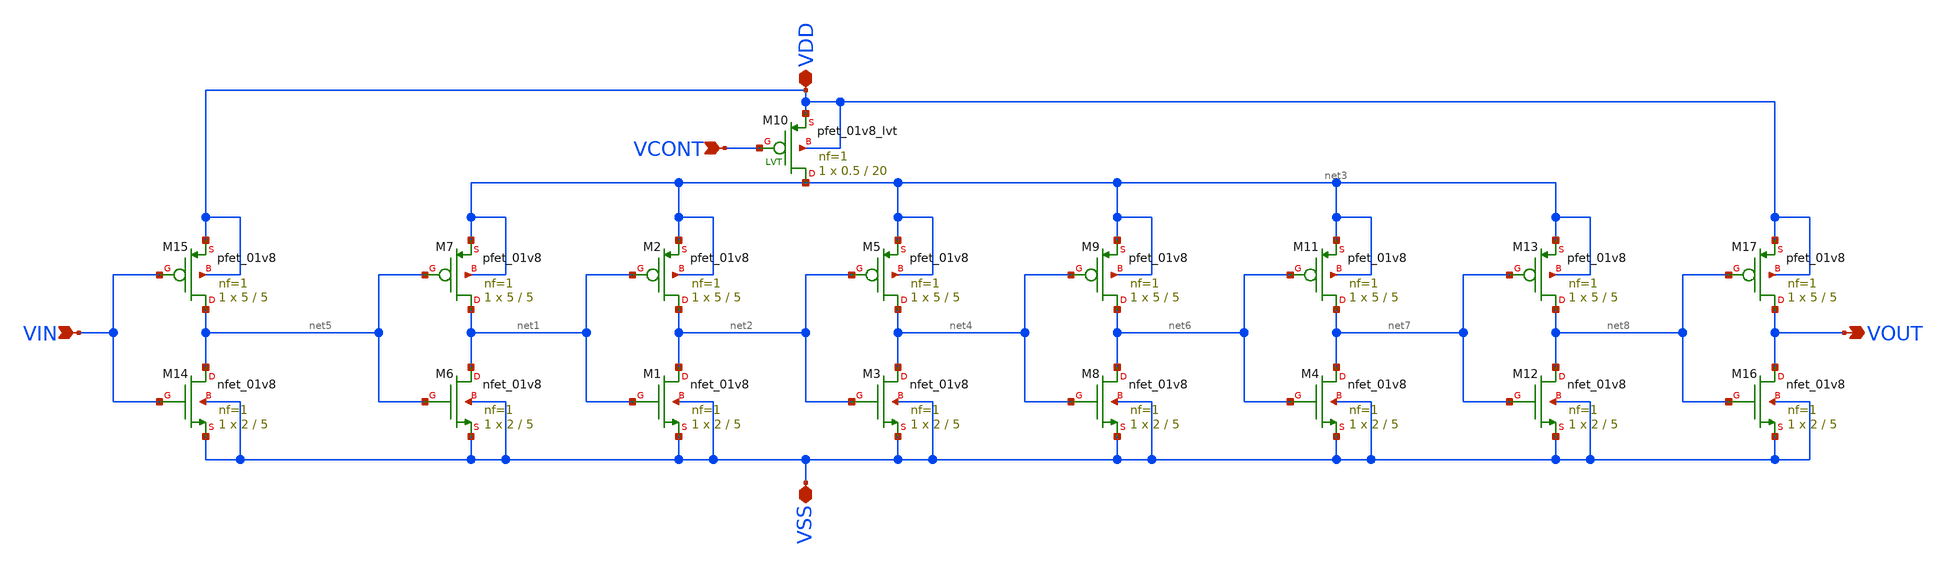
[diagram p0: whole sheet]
** sch_path: xschem/VCDL_HD_v2p1.sch
**.subckt VCDL_HD_v2p1 VIN VOUT VDD VSS VCONT
*.ipin VIN
*.opin VOUT
*.iopin VDD
*.iopin VSS
*.ipin VCONT
XM1 net2 net1 VSS VSS sky130_fd_pr__nfet_01v8 L=5 W=2 nf=1 ad='int((nf+1)/2) * W/nf * 0.29' as='int((nf+2)/2) * W/nf * 0.29'
+ pd='2*int((nf+1)/2) * (W/nf + 0.29)' ps='2*int((nf+2)/2) * (W/nf + 0.29)' nrd='0.29 / W' nrs='0.29 / W'
+ sa=0 sb=0 sd=0 mult=1 m=1
XM2 net2 net1 net3 net3 sky130_fd_pr__pfet_01v8 L=5 W=5 nf=1 ad='int((nf+1)/2) * W/nf * 0.29' as='int((nf+2)/2) * W/nf * 0.29'
+ pd='2*int((nf+1)/2) * (W/nf + 0.29)' ps='2*int((nf+2)/2) * (W/nf + 0.29)' nrd='0.29 / W' nrs='0.29 / W'
+ sa=0 sb=0 sd=0 mult=1 m=1
XM3 net4 net2 VSS VSS sky130_fd_pr__nfet_01v8 L=5 W=2 nf=1 ad='int((nf+1)/2) * W/nf * 0.29' as='int((nf+2)/2) * W/nf * 0.29'
+ pd='2*int((nf+1)/2) * (W/nf + 0.29)' ps='2*int((nf+2)/2) * (W/nf + 0.29)' nrd='0.29 / W' nrs='0.29 / W'
+ sa=0 sb=0 sd=0 mult=1 m=1
XM5 net4 net2 net3 net3 sky130_fd_pr__pfet_01v8 L=5 W=5 nf=1 ad='int((nf+1)/2) * W/nf * 0.29' as='int((nf+2)/2) * W/nf * 0.29'
+ pd='2*int((nf+1)/2) * (W/nf + 0.29)' ps='2*int((nf+2)/2) * (W/nf + 0.29)' nrd='0.29 / W' nrs='0.29 / W'
+ sa=0 sb=0 sd=0 mult=1 m=1
XM6 net1 net5 VSS VSS sky130_fd_pr__nfet_01v8 L=5 W=2 nf=1 ad='int((nf+1)/2) * W/nf * 0.29' as='int((nf+2)/2) * W/nf * 0.29'
+ pd='2*int((nf+1)/2) * (W/nf + 0.29)' ps='2*int((nf+2)/2) * (W/nf + 0.29)' nrd='0.29 / W' nrs='0.29 / W'
+ sa=0 sb=0 sd=0 mult=1 m=1
XM7 net1 net5 net3 net3 sky130_fd_pr__pfet_01v8 L=5 W=5 nf=1 ad='int((nf+1)/2) * W/nf * 0.29' as='int((nf+2)/2) * W/nf * 0.29'
+ pd='2*int((nf+1)/2) * (W/nf + 0.29)' ps='2*int((nf+2)/2) * (W/nf + 0.29)' nrd='0.29 / W' nrs='0.29 / W'
+ sa=0 sb=0 sd=0 mult=1 m=1
XM8 net6 net4 VSS VSS sky130_fd_pr__nfet_01v8 L=5 W=2 nf=1 ad='int((nf+1)/2) * W/nf * 0.29' as='int((nf+2)/2) * W/nf * 0.29'
+ pd='2*int((nf+1)/2) * (W/nf + 0.29)' ps='2*int((nf+2)/2) * (W/nf + 0.29)' nrd='0.29 / W' nrs='0.29 / W'
+ sa=0 sb=0 sd=0 mult=1 m=1
XM9 net6 net4 net3 net3 sky130_fd_pr__pfet_01v8 L=5 W=5 nf=1 ad='int((nf+1)/2) * W/nf * 0.29' as='int((nf+2)/2) * W/nf * 0.29'
+ pd='2*int((nf+1)/2) * (W/nf + 0.29)' ps='2*int((nf+2)/2) * (W/nf + 0.29)' nrd='0.29 / W' nrs='0.29 / W'
+ sa=0 sb=0 sd=0 mult=1 m=1
XM10 net3 VCONT VDD VDD sky130_fd_pr__pfet_01v8_lvt L=20 W=0.5 nf=1 ad='int((nf+1)/2) * W/nf * 0.29'
+ as='int((nf+2)/2) * W/nf * 0.29' pd='2*int((nf+1)/2) * (W/nf + 0.29)' ps='2*int((nf+2)/2) * (W/nf + 0.29)'
+ nrd='0.29 / W' nrs='0.29 / W' sa=0 sb=0 sd=0 mult=1 m=1
XM4 net7 net6 VSS VSS sky130_fd_pr__nfet_01v8 L=5 W=2 nf=1 ad='int((nf+1)/2) * W/nf * 0.29' as='int((nf+2)/2) * W/nf * 0.29'
+ pd='2*int((nf+1)/2) * (W/nf + 0.29)' ps='2*int((nf+2)/2) * (W/nf + 0.29)' nrd='0.29 / W' nrs='0.29 / W'
+ sa=0 sb=0 sd=0 mult=1 m=1
XM11 net7 net6 net3 net3 sky130_fd_pr__pfet_01v8 L=5 W=5 nf=1 ad='int((nf+1)/2) * W/nf * 0.29' as='int((nf+2)/2) * W/nf * 0.29'
+ pd='2*int((nf+1)/2) * (W/nf + 0.29)' ps='2*int((nf+2)/2) * (W/nf + 0.29)' nrd='0.29 / W' nrs='0.29 / W'
+ sa=0 sb=0 sd=0 mult=1 m=1
XM12 net8 net7 VSS VSS sky130_fd_pr__nfet_01v8 L=5 W=2 nf=1 ad='int((nf+1)/2) * W/nf * 0.29' as='int((nf+2)/2) * W/nf * 0.29'
+ pd='2*int((nf+1)/2) * (W/nf + 0.29)' ps='2*int((nf+2)/2) * (W/nf + 0.29)' nrd='0.29 / W' nrs='0.29 / W'
+ sa=0 sb=0 sd=0 mult=1 m=1
XM13 net8 net7 net3 net3 sky130_fd_pr__pfet_01v8 L=5 W=5 nf=1 ad='int((nf+1)/2) * W/nf * 0.29' as='int((nf+2)/2) * W/nf * 0.29'
+ pd='2*int((nf+1)/2) * (W/nf + 0.29)' ps='2*int((nf+2)/2) * (W/nf + 0.29)' nrd='0.29 / W' nrs='0.29 / W'
+ sa=0 sb=0 sd=0 mult=1 m=1
XM14 net5 VIN VSS VSS sky130_fd_pr__nfet_01v8 L=5 W=2 nf=1 ad='int((nf+1)/2) * W/nf * 0.29' as='int((nf+2)/2) * W/nf * 0.29'
+ pd='2*int((nf+1)/2) * (W/nf + 0.29)' ps='2*int((nf+2)/2) * (W/nf + 0.29)' nrd='0.29 / W' nrs='0.29 / W'
+ sa=0 sb=0 sd=0 mult=1 m=1
XM15 net5 VIN VDD VDD sky130_fd_pr__pfet_01v8 L=5 W=5 nf=1 ad='int((nf+1)/2) * W/nf * 0.29' as='int((nf+2)/2) * W/nf * 0.29'
+ pd='2*int((nf+1)/2) * (W/nf + 0.29)' ps='2*int((nf+2)/2) * (W/nf + 0.29)' nrd='0.29 / W' nrs='0.29 / W'
+ sa=0 sb=0 sd=0 mult=1 m=1
XM16 VOUT net8 VSS VSS sky130_fd_pr__nfet_01v8 L=5 W=2 nf=1 ad='int((nf+1)/2) * W/nf * 0.29' as='int((nf+2)/2) * W/nf * 0.29'
+ pd='2*int((nf+1)/2) * (W/nf + 0.29)' ps='2*int((nf+2)/2) * (W/nf + 0.29)' nrd='0.29 / W' nrs='0.29 / W'
+ sa=0 sb=0 sd=0 mult=1 m=1
XM17 VOUT net8 VDD VDD sky130_fd_pr__pfet_01v8 L=5 W=5 nf=1 ad='int((nf+1)/2) * W/nf * 0.29' as='int((nf+2)/2) * W/nf * 0.29'
+ pd='2*int((nf+1)/2) * (W/nf + 0.29)' ps='2*int((nf+2)/2) * (W/nf + 0.29)' nrd='0.29 / W' nrs='0.29 / W'
+ sa=0 sb=0 sd=0 mult=1 m=1
**.ends
.end
